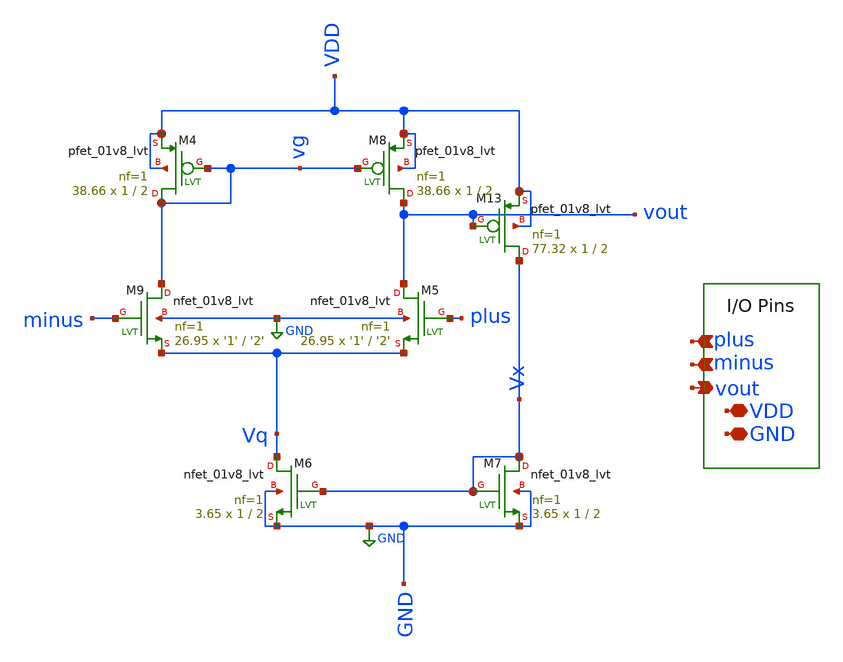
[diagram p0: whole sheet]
** sch_path: bandgap_sky130_v1/cascode_amplifier_with_bias-ckt.sch
**.subckt cascode_amplifier_with_bias-ckt plus minus vout VDD GND
*.ipin plus
*.ipin minus
*.opin vout
*.iopin VDD
*.iopin GND
XM5 vout plus Vq GND sky130_fd_pr__nfet_01v8_lvt L='2' W='1' nf=1 ad='int((nf+1)/2) * W/nf * 0.29' as='int((nf+2)/2) * W/nf * 0.29'
+ pd='2*int((nf+1)/2) * (W/nf + 0.29)' ps='2*int((nf+2)/2) * (W/nf + 0.29)' nrd='0.29 / W' nrs='0.29 / W'
+ sa=0 sb=0 sd=0 mult=26.95 m=26.95
XM6 Vq Vx GND GND sky130_fd_pr__nfet_01v8_lvt L=2 W=1 nf=1 ad='int((nf+1)/2) * W/nf * 0.29' as='int((nf+2)/2) * W/nf * 0.29'
+ pd='2*int((nf+1)/2) * (W/nf + 0.29)' ps='2*int((nf+2)/2) * (W/nf + 0.29)' nrd='0.29 / W' nrs='0.29 / W'
+ sa=0 sb=0 sd=0 mult=3.65 m=3.65
XM9 vg minus Vq GND sky130_fd_pr__nfet_01v8_lvt L='2' W='1' nf=1 ad='int((nf+1)/2) * W/nf * 0.29' as='int((nf+2)/2) * W/nf * 0.29'
+ pd='2*int((nf+1)/2) * (W/nf + 0.29)' ps='2*int((nf+2)/2) * (W/nf + 0.29)' nrd='0.29 / W' nrs='0.29 / W'
+ sa=0 sb=0 sd=0 mult=26.95 m=26.95
XM7 Vx Vx GND GND sky130_fd_pr__nfet_01v8_lvt L=2 W=1 nf=1 ad='int((nf+1)/2) * W/nf * 0.29' as='int((nf+2)/2) * W/nf * 0.29'
+ pd='2*int((nf+1)/2) * (W/nf + 0.29)' ps='2*int((nf+2)/2) * (W/nf + 0.29)' nrd='0.29 / W' nrs='0.29 / W'
+ sa=0 sb=0 sd=0 mult=3.65 m=3.65
XM13 Vx vout VDD VDD sky130_fd_pr__pfet_01v8_lvt L=2 W=1 nf=1 ad='int((nf+1)/2) * W/nf * 0.29' as='int((nf+2)/2) * W/nf * 0.29'
+ pd='2*int((nf+1)/2) * (W/nf + 0.29)' ps='2*int((nf+2)/2) * (W/nf + 0.29)' nrd='0.29 / W' nrs='0.29 / W'
+ sa=0 sb=0 sd=0 mult=77.32 m=77.32
XM4 vg vg VDD VDD sky130_fd_pr__pfet_01v8_lvt L=2 W=1 nf=1 ad='int((nf+1)/2) * W/nf * 0.29' as='int((nf+2)/2) * W/nf * 0.29'
+ pd='2*int((nf+1)/2) * (W/nf + 0.29)' ps='2*int((nf+2)/2) * (W/nf + 0.29)' nrd='0.29 / W' nrs='0.29 / W'
+ sa=0 sb=0 sd=0 mult=38.66 m=38.66
XM8 vout vg VDD VDD sky130_fd_pr__pfet_01v8_lvt L=2 W=1 nf=1 ad='int((nf+1)/2) * W/nf * 0.29' as='int((nf+2)/2) * W/nf * 0.29'
+ pd='2*int((nf+1)/2) * (W/nf + 0.29)' ps='2*int((nf+2)/2) * (W/nf + 0.29)' nrd='0.29 / W' nrs='0.29 / W'
+ sa=0 sb=0 sd=0 mult=38.66 m=38.66
**.ends
.GLOBAL GND
.end
